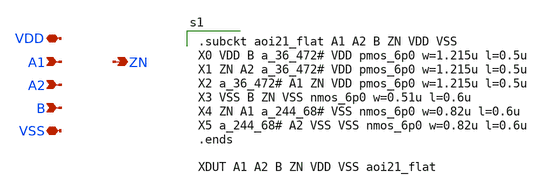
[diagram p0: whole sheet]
** sch_path: xschem/aoi21.sch
**.subckt aoi21 A1 A2 B ZN VDD VSS
*.ipin A1
*.ipin A2
*.ipin B
*.opin ZN
*.iopin VDD
*.iopin VSS
**** begin user architecture code

.subckt aoi21_flat A1 A2 B ZN VDD VSS
X0 VDD B a_36_472# VDD pmos_6p0 w=1.215u l=0.5u
X1 ZN A2 a_36_472# VDD pmos_6p0 w=1.215u l=0.5u
X2 a_36_472# A1 ZN VDD pmos_6p0 w=1.215u l=0.5u
X3 VSS B ZN VSS nmos_6p0 w=0.51u l=0.6u
X4 ZN A1 a_244_68# VSS nmos_6p0 w=0.82u l=0.6u
X5 a_244_68# A2 VSS VSS nmos_6p0 w=0.82u l=0.6u
.ends

XDUT A1 A2 B ZN VDD VSS aoi21_flat


**** end user architecture code
**.ends
.end
